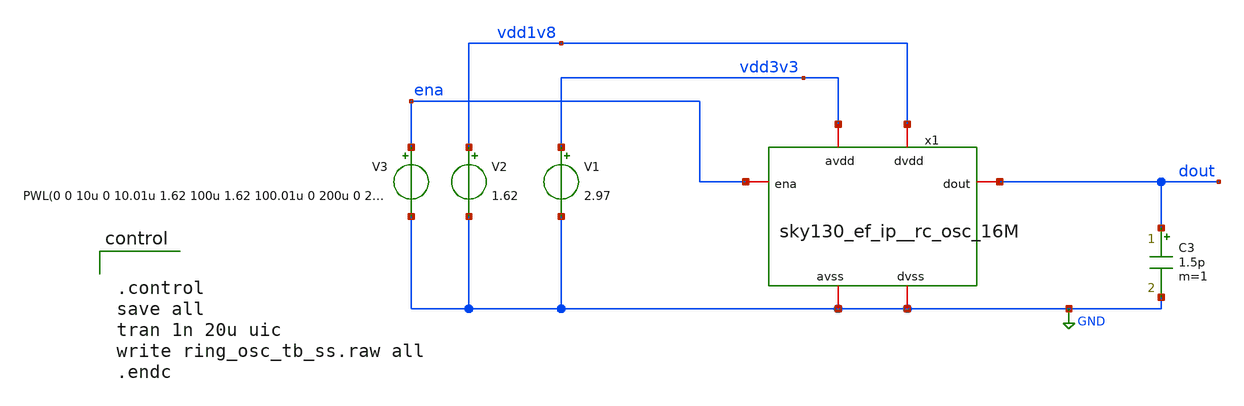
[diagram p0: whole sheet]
** sch_path: xschem/ring_osc_tb_ss.sch
**.subckt ring_osc_tb_ss
x1 ena vdd1v8 vdd3v3 GND GND dout sky130_ef_ip__rc_osc_16M
V1 vdd3v3 GND 2.97
V2 vdd1v8 GND 1.62
C3 dout GND 1.5p m=1
V3 ena GND PWL(0 0 10u 0 10.01u 1.62 100u 1.62 100.01u 0 200u 0 200.01u 1.62)
**** begin user architecture code


.option TEMP=100
.lib /usr/share/pdk/sky130A/libs.tech/ngspice/sky130.lib.spice ss




.control
save all
tran 1n 20u uic
write ring_osc_tb_ss.raw all
.endc


**** end user architecture code
**.ends
.GLOBAL GND
.end
